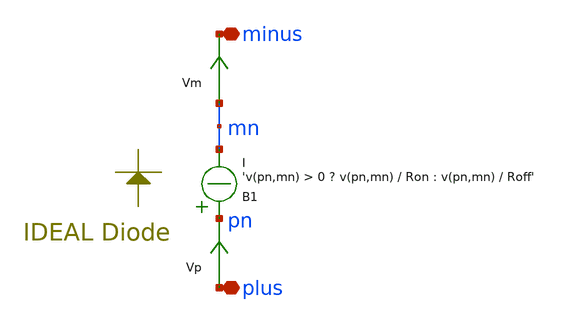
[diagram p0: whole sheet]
** sch_path: sky130A/xschem_libs/sky130_tests/diode_ngspice/schematic/diode_ngspice.sch
**.subckt diode_ngspice plus minus
*.iopin plus
*.iopin minus
Vm mn minus 0
.save i(vm)
Vp plus pn 0
.save i(vp)
B1 pn mn I = 'v(pn,mn) > 0 ? v(pn,mn) / Ron : v(pn,mn) / Roff'
**.ends
.end
